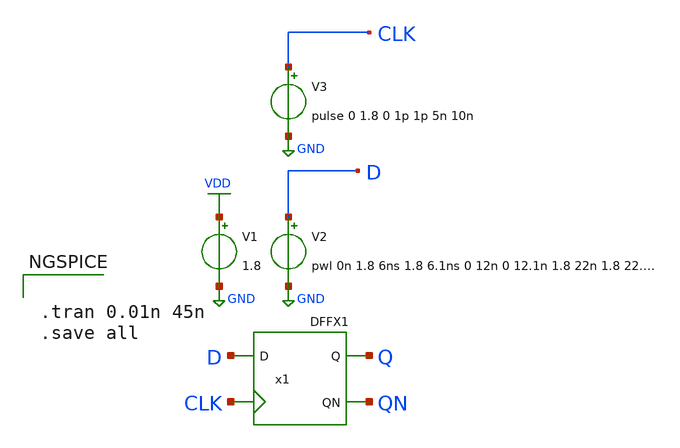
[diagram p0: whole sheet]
** sch_path: layout/xschem/sky130_rhbd/testbenches/test_DFFX1.sch
**.subckt test_DFFX1
V2 D GND pwl 0n 1.8 6ns 1.8 6.1ns 0 12n 0 12.1n 1.8 22n 1.8 22.1n 0 27n 0 27.1n 1.8 34n 1.8 34.1n 0
V1 VDD GND 1.8
V3 CLK GND pulse 0 1.8 0 1p 1p 5n 10n
x1 Q QN D CLK VDD GND DFFX1
**** begin user architecture code

.lib $::SKYWATER_MODELS/sky130.lib.spice tt


**** end user architecture code
**.ends
.GLOBAL VDD
.GLOBAL GND
**** begin user architecture code


.tran 0.01n 45n
.save all


**** end user architecture code
.end
